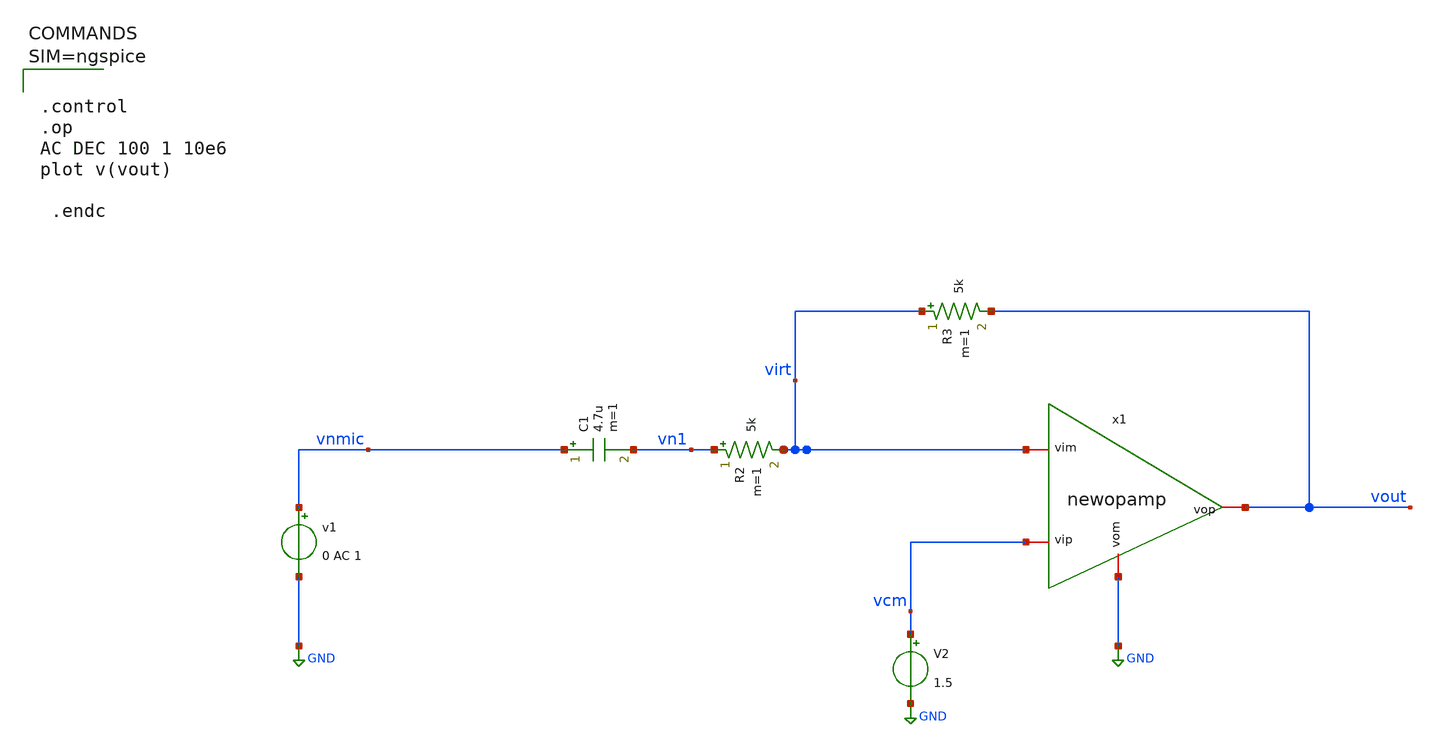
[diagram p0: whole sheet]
** sch_path: xschem/mictest2.sch
**.subckt mictest2
v1 vnmic GND 0 AC 1
R2 vn1 virt 5k m=1
R3 virt vout 5k m=1
V2 vcm GND 1.5
C1 vnmic vn1 4.7u m=1
x1 vout vcm virt GND newopamp
**** begin user architecture code



.control
.op
AC DEC 100 1 10e6
plot v(vout)

 .endc



**** end user architecture code
**.ends

* expanding   symbol:  newopamp.sym # of pins=4
** sym_path: xschem/newopamp.sym
** sch_path: xschem/newopamp.sch
.subckt newopamp vop vip vim vom
*.iopin vip
*.iopin vim
*.iopin vom
*.iopin vop
E1 vop vom vip vim 1000
.ends

.GLOBAL GND
.end
